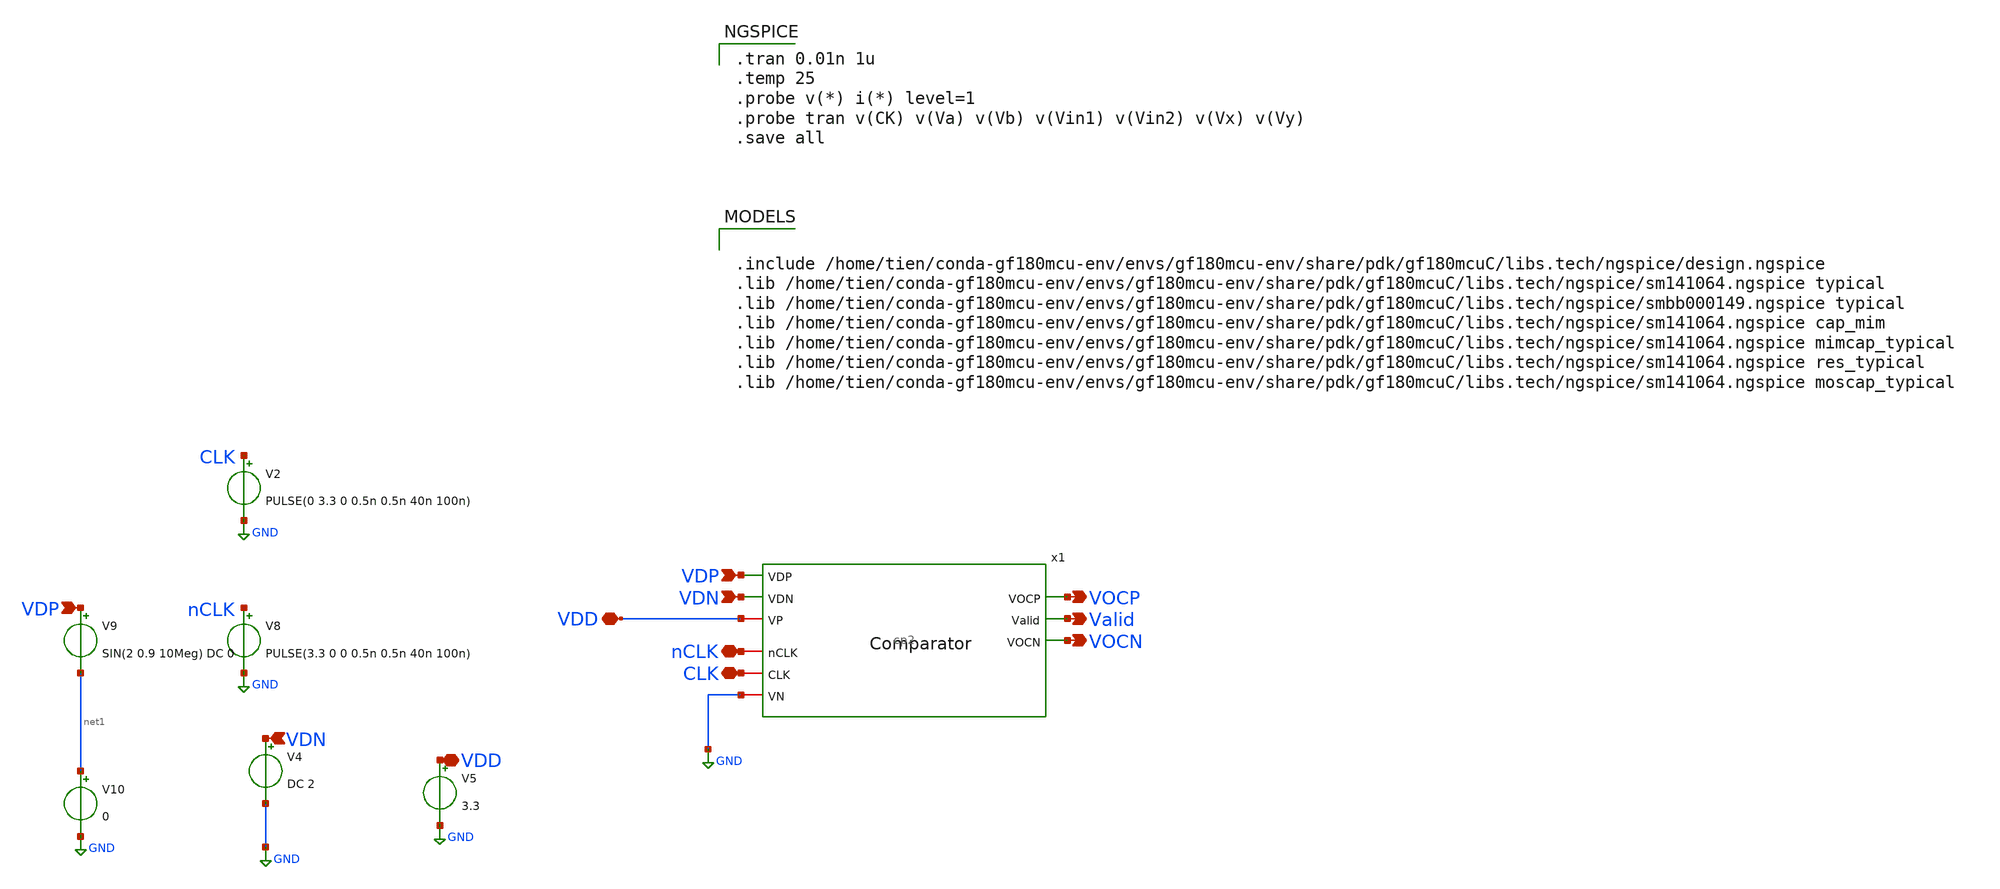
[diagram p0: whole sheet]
** sch_path: Compartor/comparator2.sch
**.subckt comparator2 Valid VOCP VOCN VDN VDD nCLK CLK VDD VDP VDN VDP
*.opin Valid
*.opin VOCP
*.opin VOCN
*.ipin VDN
*.iopin VDD
*.iopin nCLK
*.iopin CLK
*.iopin VDD
*.ipin VDP
*.ipin VDN
*.ipin VDP
V4 VDN GND DC 2
V5 VDD GND 3.3
x1 VDD VOCP VDP VDN Valid VOCN nCLK CLK GND cp2
V2 CLK GND PULSE(0 3.3 0 0.5n 0.5n 40n 100n)

V8 nCLK GND PULSE(3.3 0 0 0.5n 0.5n 40n 100n)

V9 VDP net1 SIN(2 0.9 10Meg) DC 0
V10 net1 GND 0
**** begin user architecture code

.tran 0.01n 1u
.temp 25
.probe v(*) i(*) level=1
.probe tran v(CK) v(Va) v(Vb) v(Vin1) v(Vin2) v(Vx) v(Vy)
.save all



.include /home/tien/conda-gf180mcu-env/envs/gf180mcu-env/share/pdk/gf180mcuC/libs.tech/ngspice/design.ngspice
.lib /home/tien/conda-gf180mcu-env/envs/gf180mcu-env/share/pdk/gf180mcuC/libs.tech/ngspice/sm141064.ngspice typical
.lib /home/tien/conda-gf180mcu-env/envs/gf180mcu-env/share/pdk/gf180mcuC/libs.tech/ngspice/smbb000149.ngspice typical
.lib /home/tien/conda-gf180mcu-env/envs/gf180mcu-env/share/pdk/gf180mcuC/libs.tech/ngspice/sm141064.ngspice cap_mim
.lib /home/tien/conda-gf180mcu-env/envs/gf180mcu-env/share/pdk/gf180mcuC/libs.tech/ngspice/sm141064.ngspice mimcap_typical
.lib /home/tien/conda-gf180mcu-env/envs/gf180mcu-env/share/pdk/gf180mcuC/libs.tech/ngspice/sm141064.ngspice res_typical
.lib /home/tien/conda-gf180mcu-env/envs/gf180mcu-env/share/pdk/gf180mcuC/libs.tech/ngspice/sm141064.ngspice moscap_typical

**** end user architecture code
**.ends
.GLOBAL GND
.end
